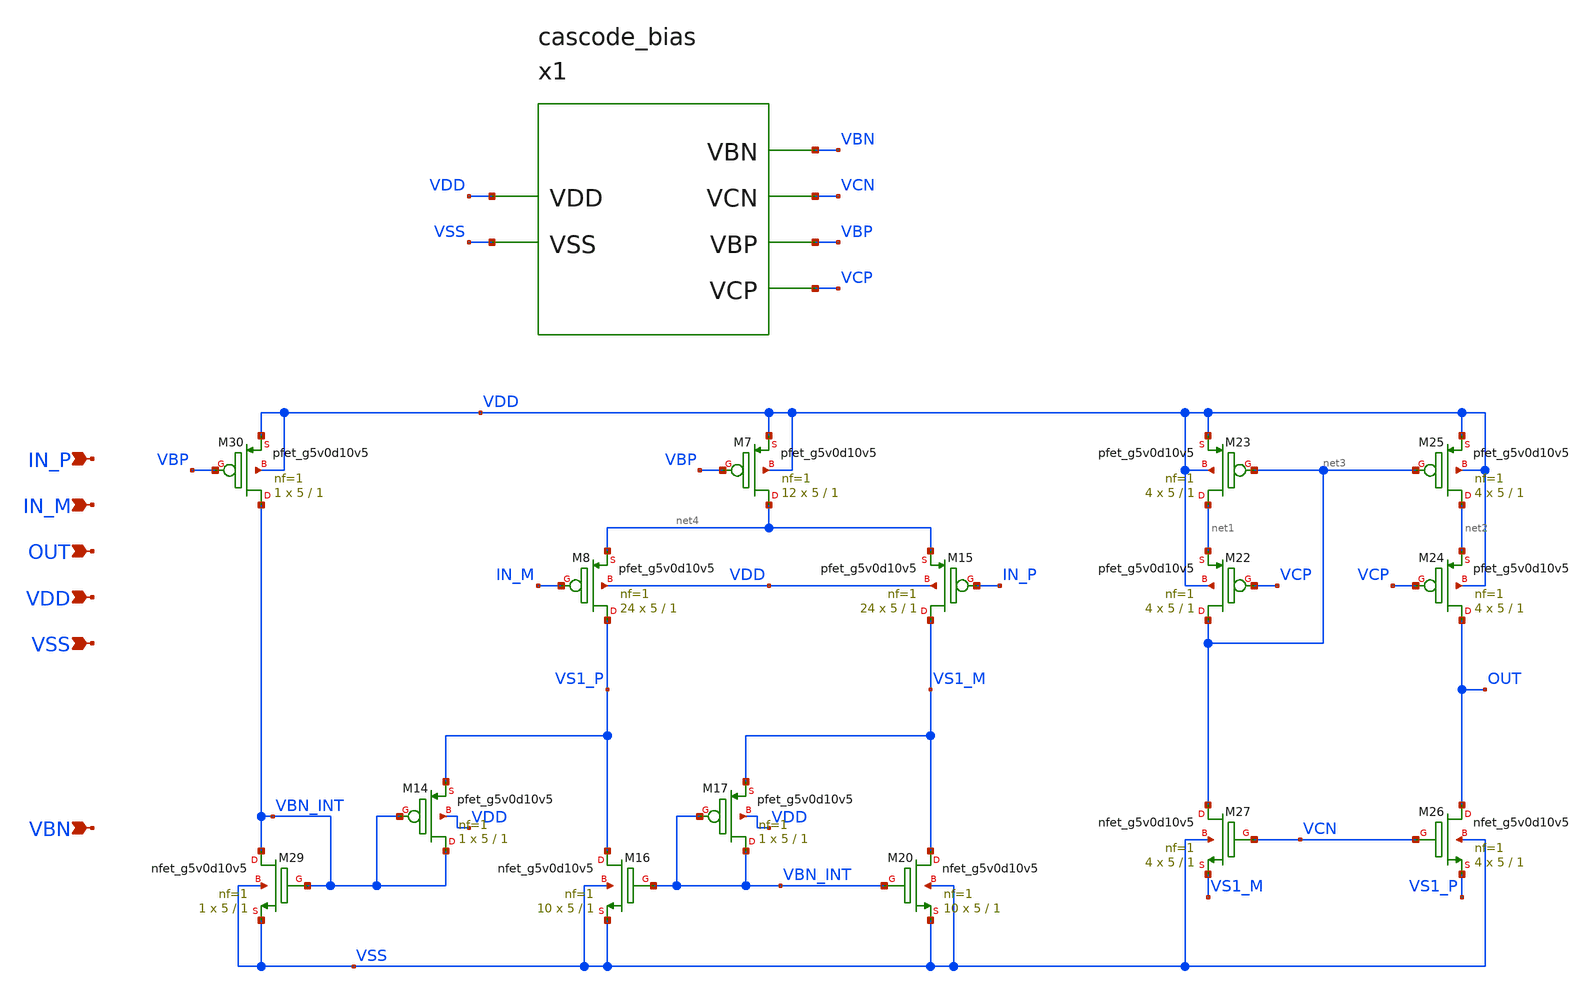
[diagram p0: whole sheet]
** sch_path: design/folded-cascode-p-in/folded_cascode_p_in.sch
**.subckt folded_cascode_p_in IN_P IN_M OUT VDD VSS VBN
*.ipin IN_P
*.ipin IN_M
*.ipin OUT
*.ipin VDD
*.ipin VSS
*.ipin VBN
XM7 net4 VBP VDD VDD sky130_fd_pr__pfet_g5v0d10v5 L=1 W=5 nf=1 ad='int((nf+1)/2) * W/nf * 0.29' as='int((nf+2)/2) * W/nf * 0.29'
+ pd='2*int((nf+1)/2) * (W/nf + 0.29)' ps='2*int((nf+2)/2) * (W/nf + 0.29)' nrd='0.29 / W' nrs='0.29 / W'
+ sa=0 sb=0 sd=0 mult=12 m=12
XM8 VS1_P IN_M net4 VDD sky130_fd_pr__pfet_g5v0d10v5 L=1 W=5 nf=1 ad='int((nf+1)/2) * W/nf * 0.29' as='int((nf+2)/2) * W/nf * 0.29'
+ pd='2*int((nf+1)/2) * (W/nf + 0.29)' ps='2*int((nf+2)/2) * (W/nf + 0.29)' nrd='0.29 / W' nrs='0.29 / W'
+ sa=0 sb=0 sd=0 mult=24 m=24
XM15 VS1_M IN_P net4 VDD sky130_fd_pr__pfet_g5v0d10v5 L=1 W=5 nf=1 ad='int((nf+1)/2) * W/nf * 0.29' as='int((nf+2)/2) * W/nf * 0.29'
+ pd='2*int((nf+1)/2) * (W/nf + 0.29)' ps='2*int((nf+2)/2) * (W/nf + 0.29)' nrd='0.29 / W' nrs='0.29 / W'
+ sa=0 sb=0 sd=0 mult=24 m=24
XM16 VS1_P VBN_INT VSS VSS sky130_fd_pr__nfet_g5v0d10v5 L=1 W=5 nf=1 ad='int((nf+1)/2) * W/nf * 0.29'
+ as='int((nf+2)/2) * W/nf * 0.29' pd='2*int((nf+1)/2) * (W/nf + 0.29)' ps='2*int((nf+2)/2) * (W/nf + 0.29)'
+ nrd='0.29 / W' nrs='0.29 / W' sa=0 sb=0 sd=0 mult=10 m=10
XM20 VS1_M VBN_INT VSS VSS sky130_fd_pr__nfet_g5v0d10v5 L=1 W=5 nf=1 ad='int((nf+1)/2) * W/nf * 0.29'
+ as='int((nf+2)/2) * W/nf * 0.29' pd='2*int((nf+1)/2) * (W/nf + 0.29)' ps='2*int((nf+2)/2) * (W/nf + 0.29)'
+ nrd='0.29 / W' nrs='0.29 / W' sa=0 sb=0 sd=0 mult=10 m=10
XM22 net3 VCP net1 VDD sky130_fd_pr__pfet_g5v0d10v5 L=1 W=5 nf=1 ad='int((nf+1)/2) * W/nf * 0.29' as='int((nf+2)/2) * W/nf * 0.29'
+ pd='2*int((nf+1)/2) * (W/nf + 0.29)' ps='2*int((nf+2)/2) * (W/nf + 0.29)' nrd='0.29 / W' nrs='0.29 / W'
+ sa=0 sb=0 sd=0 mult=4 m=4
XM23 net1 net3 VDD VDD sky130_fd_pr__pfet_g5v0d10v5 L=1 W=5 nf=1 ad='int((nf+1)/2) * W/nf * 0.29' as='int((nf+2)/2) * W/nf * 0.29'
+ pd='2*int((nf+1)/2) * (W/nf + 0.29)' ps='2*int((nf+2)/2) * (W/nf + 0.29)' nrd='0.29 / W' nrs='0.29 / W'
+ sa=0 sb=0 sd=0 mult=4 m=4
XM24 OUT VCP net2 VDD sky130_fd_pr__pfet_g5v0d10v5 L=1 W=5 nf=1 ad='int((nf+1)/2) * W/nf * 0.29' as='int((nf+2)/2) * W/nf * 0.29'
+ pd='2*int((nf+1)/2) * (W/nf + 0.29)' ps='2*int((nf+2)/2) * (W/nf + 0.29)' nrd='0.29 / W' nrs='0.29 / W'
+ sa=0 sb=0 sd=0 mult=4 m=4
XM25 net2 net3 VDD VDD sky130_fd_pr__pfet_g5v0d10v5 L=1 W=5 nf=1 ad='int((nf+1)/2) * W/nf * 0.29' as='int((nf+2)/2) * W/nf * 0.29'
+ pd='2*int((nf+1)/2) * (W/nf + 0.29)' ps='2*int((nf+2)/2) * (W/nf + 0.29)' nrd='0.29 / W' nrs='0.29 / W'
+ sa=0 sb=0 sd=0 mult=4 m=4
XM26 OUT VCN VS1_P VSS sky130_fd_pr__nfet_g5v0d10v5 L=1 W=5 nf=1 ad='int((nf+1)/2) * W/nf * 0.29' as='int((nf+2)/2) * W/nf * 0.29'
+ pd='2*int((nf+1)/2) * (W/nf + 0.29)' ps='2*int((nf+2)/2) * (W/nf + 0.29)' nrd='0.29 / W' nrs='0.29 / W'
+ sa=0 sb=0 sd=0 mult=4 m=4
XM27 net3 VCN VS1_M VSS sky130_fd_pr__nfet_g5v0d10v5 L=1 W=5 nf=1 ad='int((nf+1)/2) * W/nf * 0.29' as='int((nf+2)/2) * W/nf * 0.29'
+ pd='2*int((nf+1)/2) * (W/nf + 0.29)' ps='2*int((nf+2)/2) * (W/nf + 0.29)' nrd='0.29 / W' nrs='0.29 / W'
+ sa=0 sb=0 sd=0 mult=4 m=4
XM29 VBN_INT VBN_INT VSS VSS sky130_fd_pr__nfet_g5v0d10v5 L=1 W=5 nf=1 ad='int((nf+1)/2) * W/nf * 0.29'
+ as='int((nf+2)/2) * W/nf * 0.29' pd='2*int((nf+1)/2) * (W/nf + 0.29)' ps='2*int((nf+2)/2) * (W/nf + 0.29)'
+ nrd='0.29 / W' nrs='0.29 / W' sa=0 sb=0 sd=0 mult=1 m=1
XM30 VBN_INT VBP VDD VDD sky130_fd_pr__pfet_g5v0d10v5 L=1 W=5 nf=1 ad='int((nf+1)/2) * W/nf * 0.29' as='int((nf+2)/2) * W/nf * 0.29'
+ pd='2*int((nf+1)/2) * (W/nf + 0.29)' ps='2*int((nf+2)/2) * (W/nf + 0.29)' nrd='0.29 / W' nrs='0.29 / W'
+ sa=0 sb=0 sd=0 mult=1 m=1
XM14 VBN_INT VBN_INT VS1_P VDD sky130_fd_pr__pfet_g5v0d10v5 L=1 W=5 nf=1 ad='int((nf+1)/2) * W/nf * 0.29'
+ as='int((nf+2)/2) * W/nf * 0.29' pd='2*int((nf+1)/2) * (W/nf + 0.29)' ps='2*int((nf+2)/2) * (W/nf + 0.29)'
+ nrd='0.29 / W' nrs='0.29 / W' sa=0 sb=0 sd=0 mult=1 m=1
XM17 VBN_INT VBN_INT VS1_M VDD sky130_fd_pr__pfet_g5v0d10v5 L=1 W=5 nf=1 ad='int((nf+1)/2) * W/nf * 0.29'
+ as='int((nf+2)/2) * W/nf * 0.29' pd='2*int((nf+1)/2) * (W/nf + 0.29)' ps='2*int((nf+2)/2) * (W/nf + 0.29)'
+ nrd='0.29 / W' nrs='0.29 / W' sa=0 sb=0 sd=0 mult=1 m=1
x1 VBN VCN VBP VCP VDD VSS cascode_bias
**.ends

* expanding   symbol:  design/bias-circuit/cascode_bias.sym # of pins=6
** sym_path: design/bias-circuit/cascode_bias.sym
** sch_path: design/bias-circuit/cascode_bias.sch
.subckt cascode_bias VBN VCN VBP VCP VDD VSS
*.ipin VCN
*.ipin VBP
*.ipin VCP
*.ipin VDD
*.ipin VSS
*.ipin VBN
XM1 VBP VBP VDD VDD sky130_fd_pr__pfet_g5v0d10v5 L=1 W=5 nf=1 ad='int((nf+1)/2) * W/nf * 0.29' as='int((nf+2)/2) * W/nf * 0.29'
+ pd='2*int((nf+1)/2) * (W/nf + 0.29)' ps='2*int((nf+2)/2) * (W/nf + 0.29)' nrd='0.29 / W' nrs='0.29 / W'
+ sa=0 sb=0 sd=0 mult=1 m=1
XM2 net1 VBP net8 VDD sky130_fd_pr__pfet_g5v0d10v5 L=1 W=5 nf=1 ad='int((nf+1)/2) * W/nf * 0.29' as='int((nf+2)/2) * W/nf * 0.29'
+ pd='2*int((nf+1)/2) * (W/nf + 0.29)' ps='2*int((nf+2)/2) * (W/nf + 0.29)' nrd='0.29 / W' nrs='0.29 / W'
+ sa=0 sb=0 sd=0 mult=1 m=1
XM3 VCN VBP VDD VDD sky130_fd_pr__pfet_g5v0d10v5 L=1 W=5 nf=1 ad='int((nf+1)/2) * W/nf * 0.29' as='int((nf+2)/2) * W/nf * 0.29'
+ pd='2*int((nf+1)/2) * (W/nf + 0.29)' ps='2*int((nf+2)/2) * (W/nf + 0.29)' nrd='0.29 / W' nrs='0.29 / W'
+ sa=0 sb=0 sd=0 mult=1 m=1
XM4 net1 net1 net2 VSS sky130_fd_pr__nfet_g5v0d10v5 L=1 W=5 nf=1 ad='int((nf+1)/2) * W/nf * 0.29' as='int((nf+2)/2) * W/nf * 0.29'
+ pd='2*int((nf+1)/2) * (W/nf + 0.29)' ps='2*int((nf+2)/2) * (W/nf + 0.29)' nrd='0.29 / W' nrs='0.29 / W'
+ sa=0 sb=0 sd=0 mult=2 m=2
XM5 net2 net1 VSS VSS sky130_fd_pr__nfet_g5v0d10v5 L=1 W=5 nf=1 ad='int((nf+1)/2) * W/nf * 0.29' as='int((nf+2)/2) * W/nf * 0.29'
+ pd='2*int((nf+1)/2) * (W/nf + 0.29)' ps='2*int((nf+2)/2) * (W/nf + 0.29)' nrd='0.29 / W' nrs='0.29 / W'
+ sa=0 sb=0 sd=0 mult=1 m=1
XM21 VCN VCN net2 VSS sky130_fd_pr__nfet_g5v0d10v5 L=1 W=5 nf=1 ad='int((nf+1)/2) * W/nf * 0.29' as='int((nf+2)/2) * W/nf * 0.29'
+ pd='2*int((nf+1)/2) * (W/nf + 0.29)' ps='2*int((nf+2)/2) * (W/nf + 0.29)' nrd='0.29 / W' nrs='0.29 / W'
+ sa=0 sb=0 sd=0 mult=1 m=1
XM6 net3 VBN net6 VSS sky130_fd_pr__nfet_g5v0d10v5 L=1 W=5 nf=1 ad='int((nf+1)/2) * W/nf * 0.29' as='int((nf+2)/2) * W/nf * 0.29'
+ pd='2*int((nf+1)/2) * (W/nf + 0.29)' ps='2*int((nf+2)/2) * (W/nf + 0.29)' nrd='0.29 / W' nrs='0.29 / W'
+ sa=0 sb=0 sd=0 mult=1 m=1
XM9 VCP VBN VSS VSS sky130_fd_pr__nfet_g5v0d10v5 L=1 W=5 nf=1 ad='int((nf+1)/2) * W/nf * 0.29' as='int((nf+2)/2) * W/nf * 0.29'
+ pd='2*int((nf+1)/2) * (W/nf + 0.29)' ps='2*int((nf+2)/2) * (W/nf + 0.29)' nrd='0.29 / W' nrs='0.29 / W'
+ sa=0 sb=0 sd=0 mult=1 m=1
XM10 net3 net3 net4 VDD sky130_fd_pr__pfet_g5v0d10v5 L=1 W=5 nf=1 ad='int((nf+1)/2) * W/nf * 0.29' as='int((nf+2)/2) * W/nf * 0.29'
+ pd='2*int((nf+1)/2) * (W/nf + 0.29)' ps='2*int((nf+2)/2) * (W/nf + 0.29)' nrd='0.29 / W' nrs='0.29 / W'
+ sa=0 sb=0 sd=0 mult=2 m=2
XM11 VCP VCP net4 VDD sky130_fd_pr__pfet_g5v0d10v5 L=1 W=5 nf=1 ad='int((nf+1)/2) * W/nf * 0.29' as='int((nf+2)/2) * W/nf * 0.29'
+ pd='2*int((nf+1)/2) * (W/nf + 0.29)' ps='2*int((nf+2)/2) * (W/nf + 0.29)' nrd='0.29 / W' nrs='0.29 / W'
+ sa=0 sb=0 sd=0 mult=1 m=1
XM28 net4 net3 VDD VDD sky130_fd_pr__pfet_g5v0d10v5 L=1 W=5 nf=1 ad='int((nf+1)/2) * W/nf * 0.29' as='int((nf+2)/2) * W/nf * 0.29'
+ pd='2*int((nf+1)/2) * (W/nf + 0.29)' ps='2*int((nf+2)/2) * (W/nf + 0.29)' nrd='0.29 / W' nrs='0.29 / W'
+ sa=0 sb=0 sd=0 mult=1 m=1
XM12 VBP VBN VSS VSS sky130_fd_pr__nfet_g5v0d10v5 L=1 W=5 nf=1 ad='int((nf+1)/2) * W/nf * 0.29' as='int((nf+2)/2) * W/nf * 0.29'
+ pd='2*int((nf+1)/2) * (W/nf + 0.29)' ps='2*int((nf+2)/2) * (W/nf + 0.29)' nrd='0.29 / W' nrs='0.29 / W'
+ sa=0 sb=0 sd=0 mult=1 m=1
XM32 net8 VBP net5 VDD sky130_fd_pr__pfet_g5v0d10v5 L=1 W=5 nf=1 ad='int((nf+1)/2) * W/nf * 0.29' as='int((nf+2)/2) * W/nf * 0.29'
+ pd='2*int((nf+1)/2) * (W/nf + 0.29)' ps='2*int((nf+2)/2) * (W/nf + 0.29)' nrd='0.29 / W' nrs='0.29 / W'
+ sa=0 sb=0 sd=0 mult=1 m=1
XM33 net5 VBP VDD VDD sky130_fd_pr__pfet_g5v0d10v5 L=1 W=5 nf=1 ad='int((nf+1)/2) * W/nf * 0.29' as='int((nf+2)/2) * W/nf * 0.29'
+ pd='2*int((nf+1)/2) * (W/nf + 0.29)' ps='2*int((nf+2)/2) * (W/nf + 0.29)' nrd='0.29 / W' nrs='0.29 / W'
+ sa=0 sb=0 sd=0 mult=1 m=1
XM34 net6 VBN net7 VSS sky130_fd_pr__nfet_g5v0d10v5 L=1 W=5 nf=1 ad='int((nf+1)/2) * W/nf * 0.29' as='int((nf+2)/2) * W/nf * 0.29'
+ pd='2*int((nf+1)/2) * (W/nf + 0.29)' ps='2*int((nf+2)/2) * (W/nf + 0.29)' nrd='0.29 / W' nrs='0.29 / W'
+ sa=0 sb=0 sd=0 mult=1 m=1
XM35 net7 VBN VSS VSS sky130_fd_pr__nfet_g5v0d10v5 L=1 W=5 nf=1 ad='int((nf+1)/2) * W/nf * 0.29' as='int((nf+2)/2) * W/nf * 0.29'
+ pd='2*int((nf+1)/2) * (W/nf + 0.29)' ps='2*int((nf+2)/2) * (W/nf + 0.29)' nrd='0.29 / W' nrs='0.29 / W'
+ sa=0 sb=0 sd=0 mult=1 m=1
XM13 VBN VBN VSS VSS sky130_fd_pr__nfet_g5v0d10v5 L=1 W=5 nf=1 ad='int((nf+1)/2) * W/nf * 0.29' as='int((nf+2)/2) * W/nf * 0.29'
+ pd='2*int((nf+1)/2) * (W/nf + 0.29)' ps='2*int((nf+2)/2) * (W/nf + 0.29)' nrd='0.29 / W' nrs='0.29 / W'
+ sa=0 sb=0 sd=0 mult=1 m=1
.ends

.end
